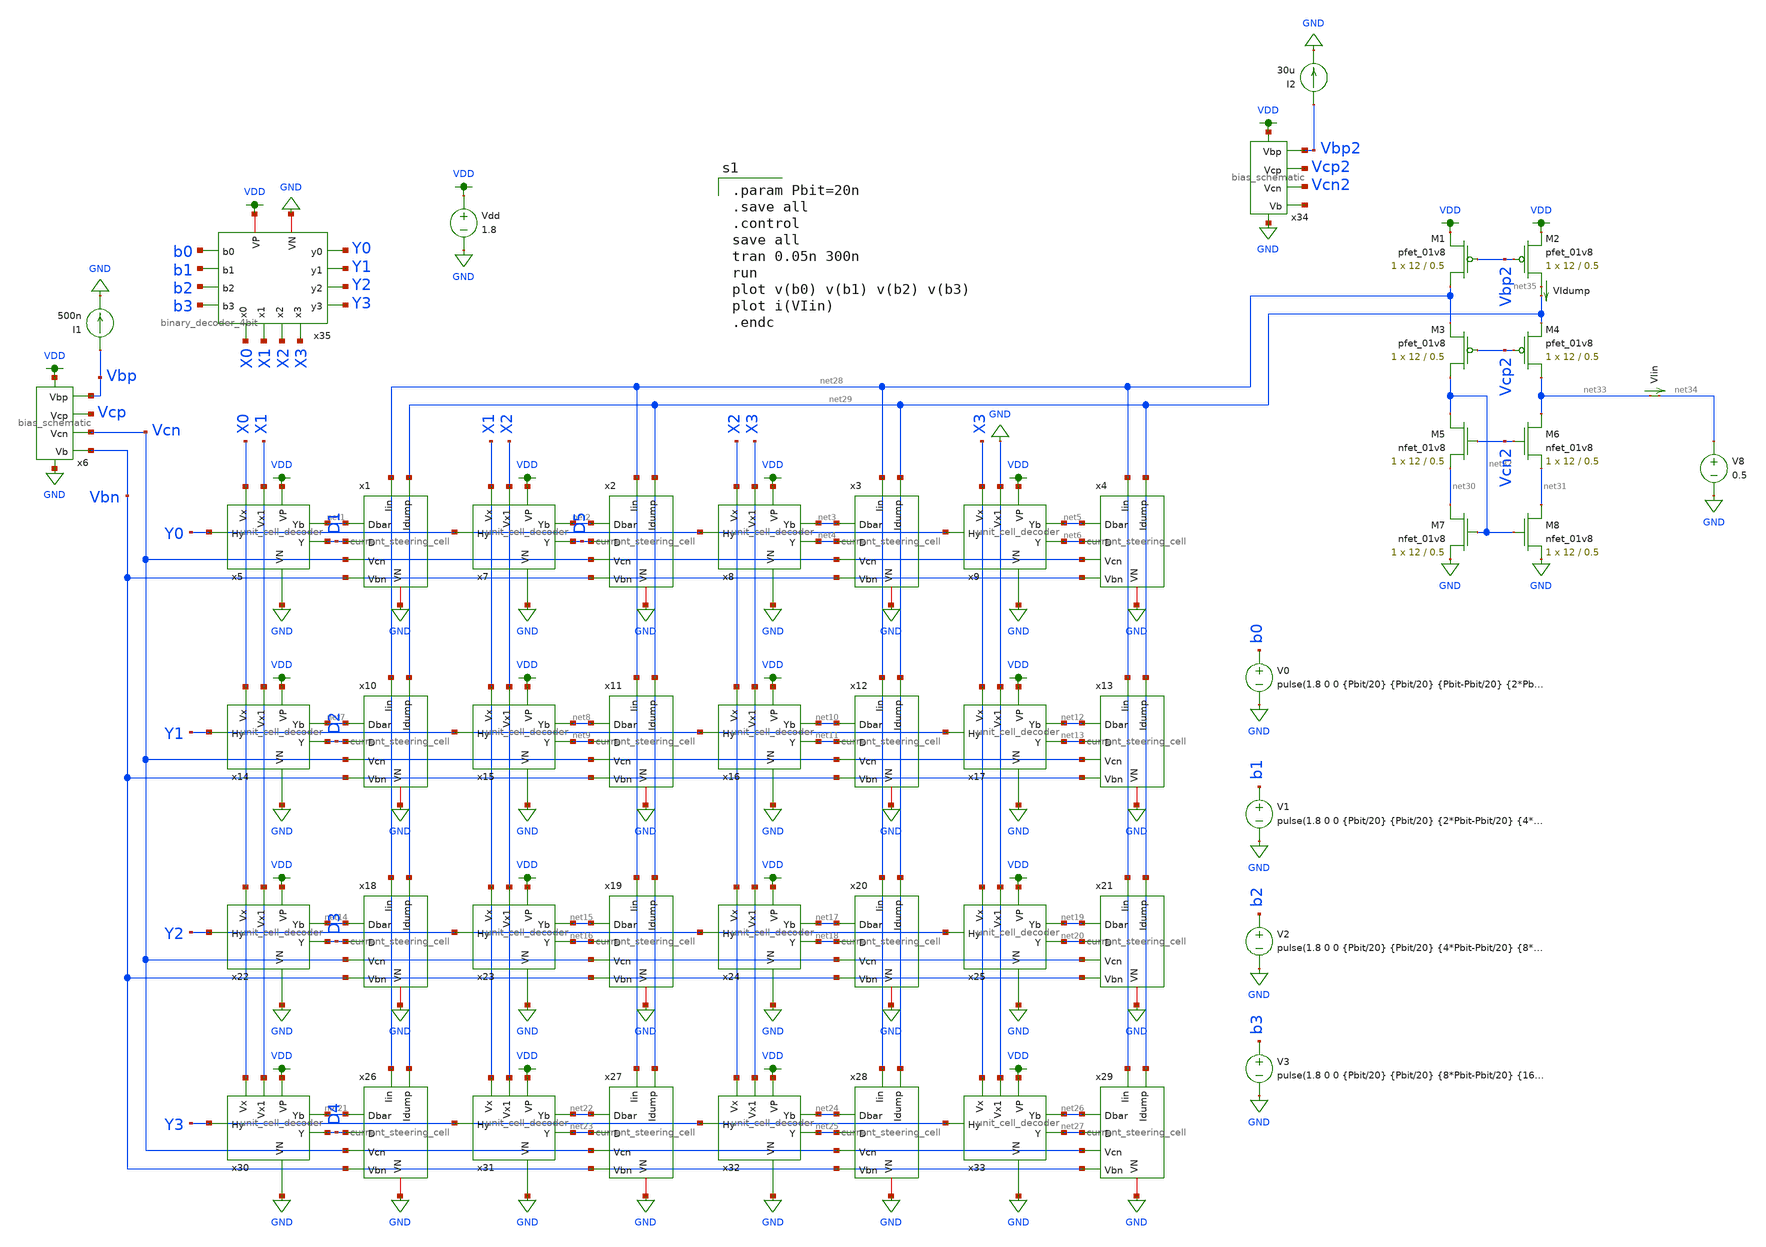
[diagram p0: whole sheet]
** sch_path: xschem/current_steering_testbenches/current_steering_testbench_transient_code_sweep.sch
**.subckt current_steering_testbench_transient_code_sweep
V1 b1 GND pulse(1.8 0 0 {Pbit/20} {Pbit/20} {2*Pbit-Pbit/20} {4*Pbit}
V2 b2 GND pulse(1.8 0 0 {Pbit/20} {Pbit/20} {4*Pbit-Pbit/20} {8*Pbit}
V3 b3 GND pulse(1.8 0 0 {Pbit/20} {Pbit/20} {8*Pbit-Pbit/20} {16*Pbit}
I1 Vbp GND 500n
VIin net33 net34 0
.save i(viin)
Vdd VDD GND 1.8
XM1 net28 Vbp2 VDD VDD sky130_fd_pr__pfet_01v8 L=0.5 W=12 nf=1 ad='int((nf+1)/2) * W/nf * 0.29' as='int((nf+2)/2) * W/nf * 0.29'
+ pd='2*int((nf+1)/2) * (W/nf + 0.29)' ps='2*int((nf+2)/2) * (W/nf + 0.29)' nrd='0.29 / W' nrs='0.29 / W'
+ sa=0 sb=0 sd=0 mult=1 m=1
XM2 net35 Vbp2 VDD VDD sky130_fd_pr__pfet_01v8 L=0.5 W=12 nf=1 ad='int((nf+1)/2) * W/nf * 0.29' as='int((nf+2)/2) * W/nf * 0.29'
+ pd='2*int((nf+1)/2) * (W/nf + 0.29)' ps='2*int((nf+2)/2) * (W/nf + 0.29)' nrd='0.29 / W' nrs='0.29 / W'
+ sa=0 sb=0 sd=0 mult=1 m=1
XM3 net32 Vcp2 net28 VDD sky130_fd_pr__pfet_01v8 L=0.5 W=12 nf=1 ad='int((nf+1)/2) * W/nf * 0.29' as='int((nf+2)/2) * W/nf * 0.29'
+ pd='2*int((nf+1)/2) * (W/nf + 0.29)' ps='2*int((nf+2)/2) * (W/nf + 0.29)' nrd='0.29 / W' nrs='0.29 / W'
+ sa=0 sb=0 sd=0 mult=1 m=1
XM4 net33 Vcp2 net29 VDD sky130_fd_pr__pfet_01v8 L=0.5 W=12 nf=1 ad='int((nf+1)/2) * W/nf * 0.29' as='int((nf+2)/2) * W/nf * 0.29'
+ pd='2*int((nf+1)/2) * (W/nf + 0.29)' ps='2*int((nf+2)/2) * (W/nf + 0.29)' nrd='0.29 / W' nrs='0.29 / W'
+ sa=0 sb=0 sd=0 mult=1 m=1
V0 b0 GND pulse(1.8 0 0 {Pbit/20} {Pbit/20} {Pbit-Pbit/20} {2*Pbit}
x5 X0 X1 Y0 VDD GND net1 D1 unit_cell_decoder
x7 X1 X2 Y0 VDD GND net2 D5 unit_cell_decoder
x8 X2 X3 Y0 VDD GND net3 net4 unit_cell_decoder
x9 X3 GND Y0 VDD GND net5 net6 unit_cell_decoder
x14 X0 X1 Y1 VDD GND net7 D2 unit_cell_decoder
x15 X1 X2 Y1 VDD GND net8 net9 unit_cell_decoder
x16 X2 X3 Y1 VDD GND net10 net11 unit_cell_decoder
x17 X3 GND Y1 VDD GND net12 net13 unit_cell_decoder
x22 X0 X1 Y2 VDD GND net14 D3 unit_cell_decoder
x23 X1 X2 Y2 VDD GND net15 net16 unit_cell_decoder
x24 X2 X3 Y2 VDD GND net17 net18 unit_cell_decoder
x25 X3 GND Y2 VDD GND net19 net20 unit_cell_decoder
x30 X0 X1 Y3 VDD GND net21 D4 unit_cell_decoder
x31 X1 X2 Y3 VDD GND net22 net23 unit_cell_decoder
x32 X2 X3 Y3 VDD GND net24 net25 unit_cell_decoder
x33 X3 GND Y3 VDD GND net26 net27 unit_cell_decoder
x1 net28 net29 net1 D1 Vcn Vbn GND current_steering_cell
x2 net28 net29 net2 D5 Vcn Vbn GND current_steering_cell
x3 net28 net29 net3 net4 Vcn Vbn GND current_steering_cell
x4 net28 net29 net5 net6 Vcn Vbn GND current_steering_cell
x10 net28 net29 net7 D2 Vcn Vbn GND current_steering_cell
x11 net28 net29 net8 net9 Vcn Vbn GND current_steering_cell
x12 net28 net29 net10 net11 Vcn Vbn GND current_steering_cell
x13 net28 net29 net12 net13 Vcn Vbn GND current_steering_cell
x18 net28 net29 net14 D3 Vcn Vbn GND current_steering_cell
x19 net28 net29 net15 net16 Vcn Vbn GND current_steering_cell
x20 net28 net29 net17 net18 Vcn Vbn GND current_steering_cell
x21 net28 net29 net19 net20 Vcn Vbn GND current_steering_cell
x26 net28 net29 net21 D4 Vcn Vbn GND current_steering_cell
x27 net28 net29 net22 net23 Vcn Vbn GND current_steering_cell
x28 net28 net29 net24 net25 Vcn Vbn GND current_steering_cell
x29 net28 net29 net26 net27 Vcn Vbn GND current_steering_cell
x6 VDD Vbp Vcp Vcn GND Vbn bias_schematic
XM5 net32 Vcn2 net30 GND sky130_fd_pr__nfet_01v8 L=0.5 W=12 nf=1 ad='int((nf+1)/2) * W/nf * 0.29' as='int((nf+2)/2) * W/nf * 0.29'
+ pd='2*int((nf+1)/2) * (W/nf + 0.29)' ps='2*int((nf+2)/2) * (W/nf + 0.29)' nrd='0.29 / W' nrs='0.29 / W'
+ sa=0 sb=0 sd=0 mult=1 m=1
XM6 net33 Vcn2 net31 GND sky130_fd_pr__nfet_01v8 L=0.5 W=12 nf=1 ad='int((nf+1)/2) * W/nf * 0.29' as='int((nf+2)/2) * W/nf * 0.29'
+ pd='2*int((nf+1)/2) * (W/nf + 0.29)' ps='2*int((nf+2)/2) * (W/nf + 0.29)' nrd='0.29 / W' nrs='0.29 / W'
+ sa=0 sb=0 sd=0 mult=1 m=1
XM7 net30 net32 GND GND sky130_fd_pr__nfet_01v8 L=0.5 W=12 nf=1 ad='int((nf+1)/2) * W/nf * 0.29' as='int((nf+2)/2) * W/nf * 0.29'
+ pd='2*int((nf+1)/2) * (W/nf + 0.29)' ps='2*int((nf+2)/2) * (W/nf + 0.29)' nrd='0.29 / W' nrs='0.29 / W'
+ sa=0 sb=0 sd=0 mult=1 m=1
XM8 net31 net32 GND GND sky130_fd_pr__nfet_01v8 L=0.5 W=12 nf=1 ad='int((nf+1)/2) * W/nf * 0.29' as='int((nf+2)/2) * W/nf * 0.29'
+ pd='2*int((nf+1)/2) * (W/nf + 0.29)' ps='2*int((nf+2)/2) * (W/nf + 0.29)' nrd='0.29 / W' nrs='0.29 / W'
+ sa=0 sb=0 sd=0 mult=1 m=1
V8 net34 GND 0.5
VIdump net35 net29 0
.save i(vidump)
I2 Vbp2 GND 30u
x34 VDD Vbp2 Vcp2 Vcn2 GND net36 bias_schematic
x35 Y0 X0 X1 Y1 VDD b0 b1 X2 Y2 b2 b3 GND Y3 X3 binary_decoder_4bit
**** begin user architecture code

.option wnflag=1
.param MC_SWITCH=0.0
.lib ~/skywater/skywater-pdk/libraries/sky130_fd_pr_ngspice/latest/models/sky130.lib.spice tt


.param Pbit=20n
.save all
.control
save all
tran 0.05n 300n
run
plot v(b0) v(b1) v(b2) v(b3)
plot i(VIin)
.endc

**** end user architecture code
**.ends
.GLOBAL GND
.GLOBAL VDD
.end
